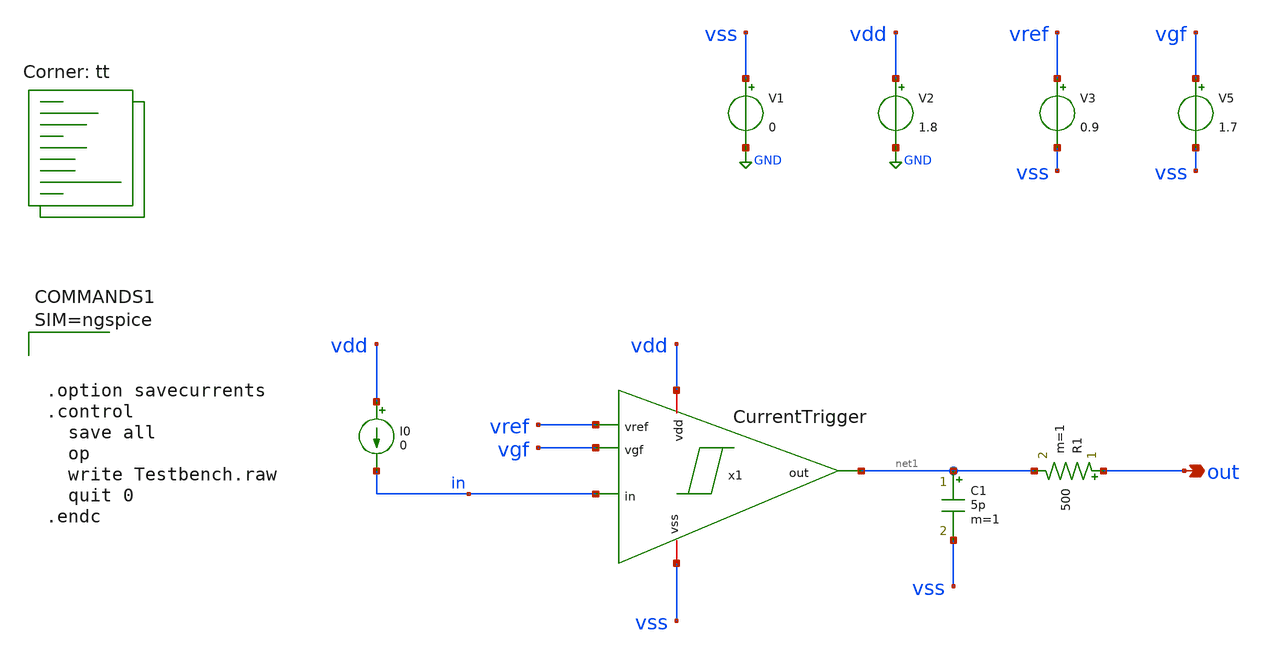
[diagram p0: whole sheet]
** sch_path: xschem/Testbench.sch
**.subckt Testbench out
*.opin out
x1 vdd vss vref vgf net1 in CurrentTrigger
V1 vss GND 0
.save i(v1)
V2 vdd GND 1.8
.save i(v2)
C1 net1 vss 5p m=1
R1 out net1 500 m=1
V3 vref vss 0.9
.save i(v3)
V5 vgf vss 1.7
.save i(v5)
I0 vdd in 0
**** begin user architecture code




.option savecurrents
.control
  save all
  op
  write Testbench.raw
  quit 0
.endc



.lib $::SKYWATER_MODELS/sky130.lib.spice tt
**** end user architecture code
**.ends

* expanding   symbol:  CurrentTrigger.sym # of pins=6
** sym_path: xschem/CurrentTrigger.sym
** sch_path: xschem/CurrentTrigger.sch
.subckt CurrentTrigger vdd vss vref vgf out in
*.iopin vdd
*.iopin vss
*.ipin in
*.opin out
*.ipin vref
*.ipin vgf
XM1 out1 g2 vss vss sky130_fd_pr__nfet_01v8_lvt L=1 W=3 nf=3 ad='int((nf+1)/2) * W/nf * 0.29' as='int((nf+2)/2) * W/nf * 0.29'
+ pd='2*int((nf+1)/2) * (W/nf + 0.29)' ps='2*int((nf+2)/2) * (W/nf + 0.29)' nrd='0.29 / W' nrs='0.29 / W'
+ sa=0 sb=0 sd=0 mult=1 m=1
XM2 g2 g2 vss vss sky130_fd_pr__nfet_01v8_lvt L=1 W=3 nf=3 ad='int((nf+1)/2) * W/nf * 0.29' as='int((nf+2)/2) * W/nf * 0.29'
+ pd='2*int((nf+1)/2) * (W/nf + 0.29)' ps='2*int((nf+2)/2) * (W/nf + 0.29)' nrd='0.29 / W' nrs='0.29 / W'
+ sa=0 sb=0 sd=0 mult=1 m=1
XM3 g2 vm in vdd sky130_fd_pr__pfet_01v8_lvt L=0.35 W=1 nf=1 ad='int((nf+1)/2) * W/nf * 0.29' as='int((nf+2)/2) * W/nf * 0.29'
+ pd='2*int((nf+1)/2) * (W/nf + 0.29)' ps='2*int((nf+2)/2) * (W/nf + 0.29)' nrd='0.29 / W' nrs='0.29 / W'
+ sa=0 sb=0 sd=0 mult=1 m=1
XM4 g1 g1 in vdd sky130_fd_pr__pfet_01v8_lvt L=0.7 W=27 nf=18 ad='int((nf+1)/2) * W/nf * 0.29' as='int((nf+2)/2) * W/nf * 0.29'
+ pd='2*int((nf+1)/2) * (W/nf + 0.29)' ps='2*int((nf+2)/2) * (W/nf + 0.29)' nrd='0.29 / W' nrs='0.29 / W'
+ sa=0 sb=0 sd=0 mult=1 m=1
XM5 vm g1 vref vdd sky130_fd_pr__pfet_01v8_lvt L=0.7 W=27 nf=18 ad='int((nf+1)/2) * W/nf * 0.29' as='int((nf+2)/2) * W/nf * 0.29'
+ pd='2*int((nf+1)/2) * (W/nf + 0.29)' ps='2*int((nf+2)/2) * (W/nf + 0.29)' nrd='0.29 / W' nrs='0.29 / W'
+ sa=0 sb=0 sd=0 mult=1 m=1
XM6 in vgb vdd vdd sky130_fd_pr__pfet_01v8_lvt L=3 W=18 nf=9 ad='int((nf+1)/2) * W/nf * 0.29' as='int((nf+2)/2) * W/nf * 0.29'
+ pd='2*int((nf+1)/2) * (W/nf + 0.29)' ps='2*int((nf+2)/2) * (W/nf + 0.29)' nrd='0.29 / W' nrs='0.29 / W'
+ sa=0 sb=0 sd=0 mult=1 m=1
XM7 net1 out1 vdd vdd sky130_fd_pr__pfet_01v8_lvt L=0.35 W=5 nf=5 ad='int((nf+1)/2) * W/nf * 0.29' as='int((nf+2)/2) * W/nf * 0.29'
+ pd='2*int((nf+1)/2) * (W/nf + 0.29)' ps='2*int((nf+2)/2) * (W/nf + 0.29)' nrd='0.29 / W' nrs='0.29 / W'
+ sa=0 sb=0 sd=0 mult=1 m=1
XM8 in vgf net1 vdd sky130_fd_pr__pfet_01v8_lvt L=2 W=3 nf=1 ad='int((nf+1)/2) * W/nf * 0.29' as='int((nf+2)/2) * W/nf * 0.29'
+ pd='2*int((nf+1)/2) * (W/nf + 0.29)' ps='2*int((nf+2)/2) * (W/nf + 0.29)' nrd='0.29 / W' nrs='0.29 / W'
+ sa=0 sb=0 sd=0 mult=1 m=1
XM9 out1 vgb vdd vdd sky130_fd_pr__pfet_01v8_lvt L=3 W=12 nf=6 ad='int((nf+1)/2) * W/nf * 0.29' as='int((nf+2)/2) * W/nf * 0.29'
+ pd='2*int((nf+1)/2) * (W/nf + 0.29)' ps='2*int((nf+2)/2) * (W/nf + 0.29)' nrd='0.29 / W' nrs='0.29 / W'
+ sa=0 sb=0 sd=0 mult=1 m=1
XM10 out2 out1 vss vss sky130_fd_pr__nfet_01v8_lvt L=0.15 W=1 nf=1 ad='int((nf+1)/2) * W/nf * 0.29' as='int((nf+2)/2) * W/nf * 0.29'
+ pd='2*int((nf+1)/2) * (W/nf + 0.29)' ps='2*int((nf+2)/2) * (W/nf + 0.29)' nrd='0.29 / W' nrs='0.29 / W'
+ sa=0 sb=0 sd=0 mult=1 m=1
XM11 out2 out1 vdd vdd sky130_fd_pr__pfet_01v8_lvt L=0.35 W=2 nf=1 ad='int((nf+1)/2) * W/nf * 0.29' as='int((nf+2)/2) * W/nf * 0.29'
+ pd='2*int((nf+1)/2) * (W/nf + 0.29)' ps='2*int((nf+2)/2) * (W/nf + 0.29)' nrd='0.29 / W' nrs='0.29 / W'
+ sa=0 sb=0 sd=0 mult=1 m=1
XM12 out3 out2 vdd vdd sky130_fd_pr__pfet_01v8_lvt L=0.35 W=6 nf=1 ad='int((nf+1)/2) * W/nf * 0.29' as='int((nf+2)/2) * W/nf * 0.29'
+ pd='2*int((nf+1)/2) * (W/nf + 0.29)' ps='2*int((nf+2)/2) * (W/nf + 0.29)' nrd='0.29 / W' nrs='0.29 / W'
+ sa=0 sb=0 sd=0 mult=1 m=1
XM13 out3 out2 vss vss sky130_fd_pr__nfet_01v8_lvt L=0.15 W=3 nf=1 ad='int((nf+1)/2) * W/nf * 0.29' as='int((nf+2)/2) * W/nf * 0.29'
+ pd='2*int((nf+1)/2) * (W/nf + 0.29)' ps='2*int((nf+2)/2) * (W/nf + 0.29)' nrd='0.29 / W' nrs='0.29 / W'
+ sa=0 sb=0 sd=0 mult=1 m=1
XM14 out out3 vdd vdd sky130_fd_pr__pfet_01v8_lvt L=0.35 W=18 nf=1 ad='int((nf+1)/2) * W/nf * 0.29' as='int((nf+2)/2) * W/nf * 0.29'
+ pd='2*int((nf+1)/2) * (W/nf + 0.29)' ps='2*int((nf+2)/2) * (W/nf + 0.29)' nrd='0.29 / W' nrs='0.29 / W'
+ sa=0 sb=0 sd=0 mult=1 m=1
XM15 out out3 vss vss sky130_fd_pr__nfet_01v8_lvt L=0.15 W=9 nf=1 ad='int((nf+1)/2) * W/nf * 0.29' as='int((nf+2)/2) * W/nf * 0.29'
+ pd='2*int((nf+1)/2) * (W/nf + 0.29)' ps='2*int((nf+2)/2) * (W/nf + 0.29)' nrd='0.29 / W' nrs='0.29 / W'
+ sa=0 sb=0 sd=0 mult=1 m=1
XM16 g1 i_n vss vss sky130_fd_pr__nfet_01v8_lvt L=3 W=12 nf=3 ad='int((nf+1)/2) * W/nf * 0.29' as='int((nf+2)/2) * W/nf * 0.29'
+ pd='2*int((nf+1)/2) * (W/nf + 0.29)' ps='2*int((nf+2)/2) * (W/nf + 0.29)' nrd='0.29 / W' nrs='0.29 / W'
+ sa=0 sb=0 sd=0 mult=1 m=1
XM17 vm i_n vss vss sky130_fd_pr__nfet_01v8_lvt L=3 W=12 nf=3 ad='int((nf+1)/2) * W/nf * 0.29' as='int((nf+2)/2) * W/nf * 0.29'
+ pd='2*int((nf+1)/2) * (W/nf + 0.29)' ps='2*int((nf+2)/2) * (W/nf + 0.29)' nrd='0.29 / W' nrs='0.29 / W'
+ sa=0 sb=0 sd=0 mult=1 m=1
XM18 i_n i_n vss vss sky130_fd_pr__nfet_01v8_lvt L=3 W=3 nf=1 ad='int((nf+1)/2) * W/nf * 0.29' as='int((nf+2)/2) * W/nf * 0.29'
+ pd='2*int((nf+1)/2) * (W/nf + 0.29)' ps='2*int((nf+2)/2) * (W/nf + 0.29)' nrd='0.29 / W' nrs='0.29 / W'
+ sa=0 sb=0 sd=0 mult=1 m=1
XM19 vgb vgb vdd vdd sky130_fd_pr__pfet_01v8_lvt L=3 W=3 nf=1 ad='int((nf+1)/2) * W/nf * 0.29' as='int((nf+2)/2) * W/nf * 0.29'
+ pd='2*int((nf+1)/2) * (W/nf + 0.29)' ps='2*int((nf+2)/2) * (W/nf + 0.29)' nrd='0.29 / W' nrs='0.29 / W'
+ sa=0 sb=0 sd=0 mult=1 m=1
XM20 net2 net2 i_n vss sky130_fd_pr__nfet_01v8_lvt L=0.15 W=21 nf=1 ad='int((nf+1)/2) * W/nf * 0.29'
+ as='int((nf+2)/2) * W/nf * 0.29' pd='2*int((nf+1)/2) * (W/nf + 0.29)' ps='2*int((nf+2)/2) * (W/nf + 0.29)'
+ nrd='0.29 / W' nrs='0.29 / W' sa=0 sb=0 sd=0 mult=1 m=1
XM21 net2 net2 vgb vdd sky130_fd_pr__pfet_01v8_lvt L=0.35 W=21 nf=1 ad='int((nf+1)/2) * W/nf * 0.29'
+ as='int((nf+2)/2) * W/nf * 0.29' pd='2*int((nf+1)/2) * (W/nf + 0.29)' ps='2*int((nf+2)/2) * (W/nf + 0.29)'
+ nrd='0.29 / W' nrs='0.29 / W' sa=0 sb=0 sd=0 mult=1 m=1
.ends

.GLOBAL GND
.end
